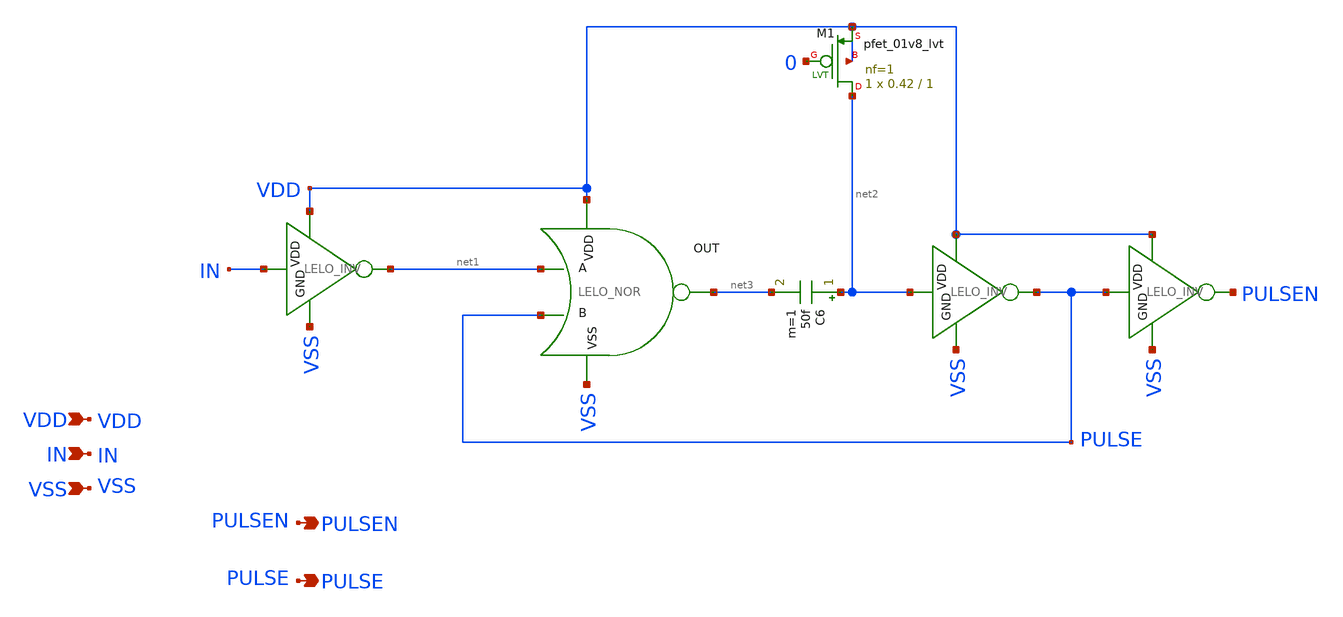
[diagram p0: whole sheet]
** sch_path: design/LELO_SVOD_SKY130A/LELO_ONESHOT.sch
**.subckt LELO_ONESHOT VDD IN VSS PULSEN PULSE
*.ipin VDD
*.ipin IN
*.ipin VSS
*.opin PULSEN
*.opin PULSE
x8 VDD PULSE PULSEN VSS LELO_INV
x12 VDD net3 net1 PULSE VSS LELO_NOR
C6 net2 net3 50f m=1
x13 VDD net2 PULSE VSS LELO_INV
x18 VDD IN net1 VSS LELO_INV
XM1 net2 0 VDD VDD sky130_fd_pr__pfet_01v8_lvt L=1 W=0.42 nf=1 ad='int((1 + 1)/2) * 0.42 / 1 * 0.29'
+ as='int((1 + 2)/2) * 0.42 / 1 * 0.29' pd='2*int((1 + 1)/2) * (0.42 / 1 + 0.29)' ps='2*int((1 + 2)/2) * (0.42 / 1 + 0.29)'
+ nrd='0.29 / 0.42 ' nrs='0.29 / 0.42 ' sa=0 sb=0 sd=0 mult=1 m=1
**.ends

* expanding   symbol:  LELO_SVOD_SKY130A/LELO_INV.sym # of pins=4
** sym_path: design/LELO_SVOD_SKY130A/LELO_INV.sym
** sch_path: design/LELO_SVOD_SKY130A/LELO_INV.sch
.subckt LELO_INV VDD VIN VOUT GND
*.ipin VIN
*.ipin VDD
*.ipin GND
*.opin VOUT
XM1 VOUT VIN GND GND sky130_fd_pr__nfet_01v8_lvt L=0.15 W=1 nf=1 ad='int((1 + 1)/2) * 1 / 1 * 0.29' as='int((1 + 2)/2) * 1 / 1 * 0.29'
+ pd='2*int((1 + 1)/2) * (1 / 1 + 0.29)' ps='2*int((1 + 2)/2) * (1 / 1 + 0.29)' nrd='0.29 / 1 ' nrs='0.29 / 1 '
+ sa=0 sb=0 sd=0 mult=1 m=1
XM2 VOUT VIN VDD VDD sky130_fd_pr__pfet_01v8_lvt L=0.35 W=1 nf=1 ad='int((1 + 1)/2) * 1 / 1 * 0.29' as='int((1 + 2)/2) * 1 / 1 * 0.29'
+ pd='2*int((1 + 1)/2) * (1 / 1 + 0.29)' ps='2*int((1 + 2)/2) * (1 / 1 + 0.29)' nrd='0.29 / 1 ' nrs='0.29 / 1 '
+ sa=0 sb=0 sd=0 mult=2 m=2
.ends


* expanding   symbol:  LELO_SVOD_SKY130A/LELO_NOR.sym # of pins=5
** sym_path: design/LELO_SVOD_SKY130A/LELO_NOR.sym
** sch_path: design/LELO_SVOD_SKY130A/LELO_NOR.sch
.subckt LELO_NOR VDD OUT A B VSS
*.ipin VDD
*.ipin VSS
*.opin OUT
*.ipin A
*.ipin B
XM5 OUT B VSS VSS sky130_fd_pr__nfet_01v8_lvt L=0.15 W=1 nf=1 ad='int((1 + 1)/2) * 1 / 1 * 0.29' as='int((1 + 2)/2) * 1 / 1 * 0.29'
+ pd='2*int((1 + 1)/2) * (1 / 1 + 0.29)' ps='2*int((1 + 2)/2) * (1 / 1 + 0.29)' nrd='0.29 / 1 ' nrs='0.29 / 1 '
+ sa=0 sb=0 sd=0 mult=1 m=1
XM6 net1 A VDD VDD sky130_fd_pr__pfet_01v8_lvt L=0.35 W=1 nf=1 ad='int((1 + 1)/2) * 1 / 1 * 0.29' as='int((1 + 2)/2) * 1 / 1 * 0.29'
+ pd='2*int((1 + 1)/2) * (1 / 1 + 0.29)' ps='2*int((1 + 2)/2) * (1 / 1 + 0.29)' nrd='0.29 / 1 ' nrs='0.29 / 1 '
+ sa=0 sb=0 sd=0 mult=4 m=4
XM3 OUT B net1 VDD sky130_fd_pr__pfet_01v8_lvt L=0.35 W=1 nf=1 ad='int((1 + 1)/2) * 1 / 1 * 0.29' as='int((1 + 2)/2) * 1 / 1 * 0.29'
+ pd='2*int((1 + 1)/2) * (1 / 1 + 0.29)' ps='2*int((1 + 2)/2) * (1 / 1 + 0.29)' nrd='0.29 / 1 ' nrs='0.29 / 1 '
+ sa=0 sb=0 sd=0 mult=4 m=4
XM1 OUT A VSS VSS sky130_fd_pr__nfet_01v8_lvt L=0.15 W=1 nf=1 ad='int((1 + 1)/2) * 1 / 1 * 0.29' as='int((1 + 2)/2) * 1 / 1 * 0.29'
+ pd='2*int((1 + 1)/2) * (1 / 1 + 0.29)' ps='2*int((1 + 2)/2) * (1 / 1 + 0.29)' nrd='0.29 / 1 ' nrs='0.29 / 1 '
+ sa=0 sb=0 sd=0 mult=1 m=1
.ends

.end
